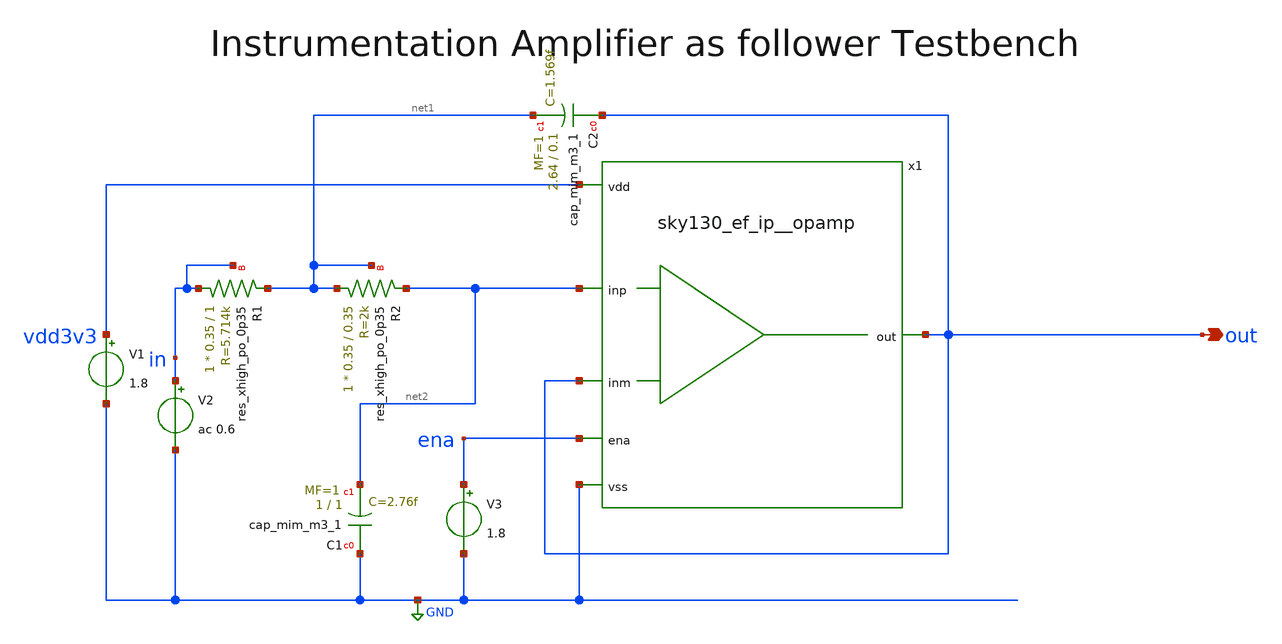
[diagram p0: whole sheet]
** sch_path: xschem/analog_desing/Filtro/sky130_ef_ip__opamp_tbcb.sch
**.subckt sky130_ef_ip__opamp_tbcb out
*.opin out
V1 vdd3v3 GND 1.8
V2 in GND ac 0.6
x1 vdd3v3 out ena GND net2 out sky130_ef_ip__opamp
V3 ena GND 1.8
XC2 out net1 sky130_fd_pr__cap_mim_m3_1 W=2.64 L=0.1 MF=1 m=1
XR1 in net1 in sky130_fd_pr__res_xhigh_po_0p35 L=1 mult=1 m=1
XR2 net1 net2 net1 sky130_fd_pr__res_xhigh_po_0p35 L=0.35 mult=1 m=1
XC1 GND net2 sky130_fd_pr__cap_mim_m3_1 W=1 L=1 MF=1 m=1
**** begin user architecture code

.lib /usr/local/share/pdk/sky130A/libs.tech/combined/sky130.lib.spice tt


.control
ac lin 10000 1 5MEG
plot db(V(out)/V(in))
.endc

**** end user architecture code
**.ends

* expanding   symbol:  sky130_ef_ip__opamp.sym # of pins=6
** sym_path: sky130_ef_ip__opamp.sym
** sch_path: sky130_ef_ip__opamp.sch
.subckt sky130_ef_ip__opamp vdd out ena vss inp inm
*.ipin vdd
*.ipin vss
*.opin out
*.ipin inm
*.ipin inp
*.ipin ena
XM4 pdrv1 net1 vdd vdd sky130_fd_pr__pfet_g5v0d10v5 L=0.5 W=2 nf=2 ad='int((nf+1)/2) * W/nf * 0.29' as='int((nf+2)/2) * W/nf * 0.29'
+ pd='2*int((nf+1)/2) * (W/nf + 0.29)' ps='2*int((nf+2)/2) * (W/nf + 0.29)' nrd='0.29 / W' nrs='0.29 / W'
+ sa=0 sb=0 sd=0 mult=1 m=1
XM5 vdd net1 net1 vdd sky130_fd_pr__pfet_g5v0d10v5 L=0.5 W=2 nf=2 ad='int((nf+1)/2) * W/nf * 0.29' as='int((nf+2)/2) * W/nf * 0.29'
+ pd='2*int((nf+1)/2) * (W/nf + 0.29)' ps='2*int((nf+2)/2) * (W/nf + 0.29)' nrd='0.29 / W' nrs='0.29 / W'
+ sa=0 sb=0 sd=0 mult=1 m=1
XM9 vcomn1 nbias vss GND sky130_fd_pr__nfet_g5v0d10v5 L=0.5 W=1 nf=1 ad='int((nf+1)/2) * W/nf * 0.29'
+ as='int((nf+2)/2) * W/nf * 0.29' pd='2*int((nf+1)/2) * (W/nf + 0.29)' ps='2*int((nf+2)/2) * (W/nf + 0.29)'
+ nrd='0.29 / W' nrs='0.29 / W' sa=0 sb=0 sd=0 mult=1 m=1
XM10 vss nbias nbias GND sky130_fd_pr__nfet_g5v0d10v5 L=0.5 W=4 nf=4 ad='int((nf+1)/2) * W/nf * 0.29'
+ as='int((nf+2)/2) * W/nf * 0.29' pd='2*int((nf+1)/2) * (W/nf + 0.29)' ps='2*int((nf+2)/2) * (W/nf + 0.29)'
+ nrd='0.29 / W' nrs='0.29 / W' sa=0 sb=0 sd=0 mult=1 m=1
XR1 net4 vdd vss sky130_fd_pr__res_xhigh_po_0p35 W=1 L=100 mult=1 m=1
XM20 out pdrv1 vdd vdd sky130_fd_pr__pfet_g5v0d10v5 L=0.5 W=200 nf=200 ad='int((nf+1)/2) * W/nf * 0.29'
+ as='int((nf+2)/2) * W/nf * 0.29' pd='2*int((nf+1)/2) * (W/nf + 0.29)' ps='2*int((nf+2)/2) * (W/nf + 0.29)'
+ nrd='0.29 / W' nrs='0.29 / W' sa=0 sb=0 sd=0 mult=1 m=1
XM22 out ndrv vss GND sky130_fd_pr__nfet_g5v0d10v5 L=0.5 W=120 nf=120 ad='int((nf+1)/2) * W/nf * 0.29'
+ as='int((nf+2)/2) * W/nf * 0.29' pd='2*int((nf+1)/2) * (W/nf + 0.29)' ps='2*int((nf+2)/2) * (W/nf + 0.29)'
+ nrd='0.29 / W' nrs='0.29 / W' sa=0 sb=0 sd=0 mult=1 m=1
XM24 pbias nbias vss GND sky130_fd_pr__nfet_g5v0d10v5 L=0.5 W=1 nf=1 ad='int((nf+1)/2) * W/nf * 0.29'
+ as='int((nf+2)/2) * W/nf * 0.29' pd='2*int((nf+1)/2) * (W/nf + 0.29)' ps='2*int((nf+2)/2) * (W/nf + 0.29)'
+ nrd='0.29 / W' nrs='0.29 / W' sa=0 sb=0 sd=0 mult=1 m=1
XM25 vdd pbias pbias vdd sky130_fd_pr__pfet_g5v0d10v5 L=0.5 W=1 nf=1 ad='int((nf+1)/2) * W/nf * 0.29'
+ as='int((nf+2)/2) * W/nf * 0.29' pd='2*int((nf+1)/2) * (W/nf + 0.29)' ps='2*int((nf+2)/2) * (W/nf + 0.29)'
+ nrd='0.29 / W' nrs='0.29 / W' sa=0 sb=0 sd=0 mult=1 m=1
XM26 vcomp pbias vdd vdd sky130_fd_pr__pfet_g5v0d10v5 L=0.5 W=2 nf=2 ad='int((nf+1)/2) * W/nf * 0.29'
+ as='int((nf+2)/2) * W/nf * 0.29' pd='2*int((nf+1)/2) * (W/nf + 0.29)' ps='2*int((nf+2)/2) * (W/nf + 0.29)'
+ nrd='0.29 / W' nrs='0.29 / W' sa=0 sb=0 sd=0 mult=1 m=1
XM27 net2 inm vcomp vdd sky130_fd_pr__pfet_g5v0d10v5 L=0.5 W=2 nf=2 ad='int((nf+1)/2) * W/nf * 0.29'
+ as='int((nf+2)/2) * W/nf * 0.29' pd='2*int((nf+1)/2) * (W/nf + 0.29)' ps='2*int((nf+2)/2) * (W/nf + 0.29)'
+ nrd='0.29 / W' nrs='0.29 / W' sa=0 sb=0 sd=0 mult=1 m=1
XM28 vcomp inp ndrv vdd sky130_fd_pr__pfet_g5v0d10v5 L=0.5 W=2 nf=2 ad='int((nf+1)/2) * W/nf * 0.29'
+ as='int((nf+2)/2) * W/nf * 0.29' pd='2*int((nf+1)/2) * (W/nf + 0.29)' ps='2*int((nf+2)/2) * (W/nf + 0.29)'
+ nrd='0.29 / W' nrs='0.29 / W' sa=0 sb=0 sd=0 mult=1 m=1
XM29 ndrv net2 vss GND sky130_fd_pr__nfet_g5v0d10v5 L=0.5 W=1 nf=1 ad='int((nf+1)/2) * W/nf * 0.29' as='int((nf+2)/2) * W/nf * 0.29'
+ pd='2*int((nf+1)/2) * (W/nf + 0.29)' ps='2*int((nf+2)/2) * (W/nf + 0.29)' nrd='0.29 / W' nrs='0.29 / W'
+ sa=0 sb=0 sd=0 mult=1 m=1
XM30 vss net2 net2 GND sky130_fd_pr__nfet_g5v0d10v5 L=0.5 W=1 nf=1 ad='int((nf+1)/2) * W/nf * 0.29' as='int((nf+2)/2) * W/nf * 0.29'
+ pd='2*int((nf+1)/2) * (W/nf + 0.29)' ps='2*int((nf+2)/2) * (W/nf + 0.29)' nrd='0.29 / W' nrs='0.29 / W'
+ sa=0 sb=0 sd=0 mult=1 m=1
XM1 net1 inm vcomn1 GND sky130_fd_pr__nfet_g5v0d10v5 L=0.5 W=1 nf=1 ad='int((nf+1)/2) * W/nf * 0.29'
+ as='int((nf+2)/2) * W/nf * 0.29' pd='2*int((nf+1)/2) * (W/nf + 0.29)' ps='2*int((nf+2)/2) * (W/nf + 0.29)'
+ nrd='0.29 / W' nrs='0.29 / W' sa=0 sb=0 sd=0 mult=1 m=1
XM2 vcomn1 inp pdrv1 GND sky130_fd_pr__nfet_g5v0d10v5 L=0.5 W=1 nf=1 ad='int((nf+1)/2) * W/nf * 0.29'
+ as='int((nf+2)/2) * W/nf * 0.29' pd='2*int((nf+1)/2) * (W/nf + 0.29)' ps='2*int((nf+2)/2) * (W/nf + 0.29)'
+ nrd='0.29 / W' nrs='0.29 / W' sa=0 sb=0 sd=0 mult=1 m=1
XM3 pdrv2 net3 vdd vdd sky130_fd_pr__pfet_g5v0d10v5 L=0.5 W=2 nf=2 ad='int((nf+1)/2) * W/nf * 0.29' as='int((nf+2)/2) * W/nf * 0.29'
+ pd='2*int((nf+1)/2) * (W/nf + 0.29)' ps='2*int((nf+2)/2) * (W/nf + 0.29)' nrd='0.29 / W' nrs='0.29 / W'
+ sa=0 sb=0 sd=0 mult=1 m=1
XM6 vdd net3 net3 vdd sky130_fd_pr__pfet_g5v0d10v5 L=0.5 W=2 nf=2 ad='int((nf+1)/2) * W/nf * 0.29' as='int((nf+2)/2) * W/nf * 0.29'
+ pd='2*int((nf+1)/2) * (W/nf + 0.29)' ps='2*int((nf+2)/2) * (W/nf + 0.29)' nrd='0.29 / W' nrs='0.29 / W'
+ sa=0 sb=0 sd=0 mult=1 m=1
XM7 vcomn2 nbias vss GND sky130_fd_pr__nfet_g5v0d10v5 L=0.5 W=1 nf=1 ad='int((nf+1)/2) * W/nf * 0.29'
+ as='int((nf+2)/2) * W/nf * 0.29' pd='2*int((nf+1)/2) * (W/nf + 0.29)' ps='2*int((nf+2)/2) * (W/nf + 0.29)'
+ nrd='0.29 / W' nrs='0.29 / W' sa=0 sb=0 sd=0 mult=1 m=1
XM8 net3 inm vcomn2 GND sky130_fd_pr__nfet_03v3_nvt L=0.5 W=1 nf=1 ad='int((nf+1)/2) * W/nf * 0.29' as='int((nf+2)/2) * W/nf * 0.29'
+ pd='2*int((nf+1)/2) * (W/nf + 0.29)' ps='2*int((nf+2)/2) * (W/nf + 0.29)' nrd='0.29 / W' nrs='0.29 / W'
+ sa=0 sb=0 sd=0 mult=1 m=1
XM11 vcomn2 inp pdrv2 GND sky130_fd_pr__nfet_03v3_nvt L=0.5 W=1 nf=1 ad='int((nf+1)/2) * W/nf * 0.29'
+ as='int((nf+2)/2) * W/nf * 0.29' pd='2*int((nf+1)/2) * (W/nf + 0.29)' ps='2*int((nf+2)/2) * (W/nf + 0.29)'
+ nrd='0.29 / W' nrs='0.29 / W' sa=0 sb=0 sd=0 mult=1 m=1
XM12 vdd pdrv2 out vdd sky130_fd_pr__pfet_g5v0d10v5 L=0.5 W=200 nf=200 ad='int((nf+1)/2) * W/nf * 0.29'
+ as='int((nf+2)/2) * W/nf * 0.29' pd='2*int((nf+1)/2) * (W/nf + 0.29)' ps='2*int((nf+2)/2) * (W/nf + 0.29)'
+ nrd='0.29 / W' nrs='0.29 / W' sa=0 sb=0 sd=0 mult=1 m=1
XDD1 vss inp sky130_fd_pr__diode_pw2nd_05v5 area=3.6e11 pj=4e6
XM13 net4 ena nbias GND sky130_fd_pr__nfet_g5v0d10v5 L=0.5 W=1 nf=1 ad='int((nf+1)/2) * W/nf * 0.29'
+ as='int((nf+2)/2) * W/nf * 0.29' pd='2*int((nf+1)/2) * (W/nf + 0.29)' ps='2*int((nf+2)/2) * (W/nf + 0.29)'
+ nrd='0.29 / W' nrs='0.29 / W' sa=0 sb=0 sd=0 mult=1 m=1
XDD2 vss ena sky130_fd_pr__diode_pw2nd_05v5 area=3.6e11 pj=4e6
XDD3 vss inm sky130_fd_pr__diode_pw2nd_05v5 area=3.6e11 pj=4e6
XR2 inp vss vss sky130_fd_pr__res_xhigh_po_0p35 W=1 L=0.45 mult=4 m=4
.ends

.GLOBAL GND
.end
